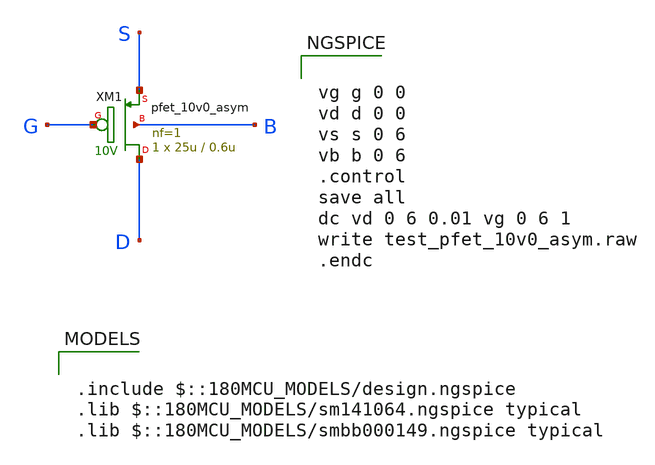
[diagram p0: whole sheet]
** sch_path: gf180mcuD/xschem_libs/gf180mcu_tests/test_pfet_10v0_asym/schematic/test_pfet_10v0_asym.sch
* Copyright 2022 GlobalFoundries PDK Authors
* Licensed under the Apache License, Version 2.0 (the "License");
* you may not use this file except in compliance with the License.
* You may obtain a copy of the License at
* https://www.apache.org/licenses/LICENSE-2.0
* Unless required by applicable law or agreed to in writing, software
* distributed under the License is distributed on an "AS IS" BASIS,
* WITHOUT WARRANTIES OR CONDITIONS OF ANY KIND, either express or implied.
* See the License for the specific language governing permissions and
* limitations under the License.
**.subckt test_pfet_10v0_asym
XM1 D G S B pfet_10v0_asym L=0.6u W=25u nf=1 ad='W * 1.78u' as='W * 0.48u' pd='2 * (W + 1.78u)' ps='2 * (W + 0.48u)'
+ nrd=0 nrs=0 sa=0 sb=0 sd=0 m=1
**** begin user architecture code


vg g 0 0
vd d 0 0
vs s 0 6
vb b 0 6
.control
save all
dc vd 0 6 0.01 vg 0 6 1
write test_pfet_10v0_asym.raw
.endc



.include $::180MCU_MODELS/design.ngspice
.lib $::180MCU_MODELS/sm141064.ngspice typical
.lib $::180MCU_MODELS/smbb000149.ngspice typical

**** end user architecture code
**.ends
.end
